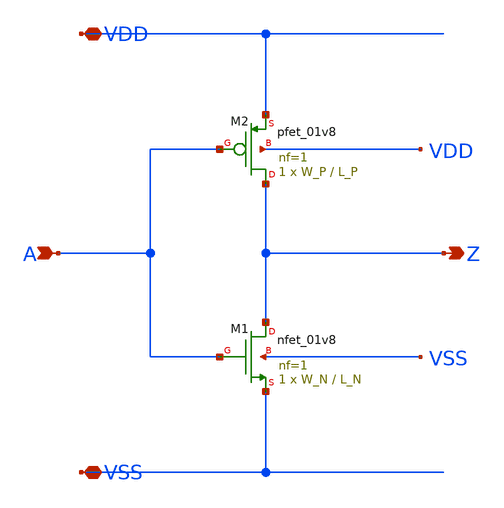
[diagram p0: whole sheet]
** sch_path: pipeline/analog/inv/inv.sch
**.subckt inv A Z VDD VSS
*.ipin A
*.opin Z
*.iopin VDD
*.iopin VSS
XM1 Z A VSS VSS sky130_fd_pr__nfet_01v8 L=L_N W=W_N nf=1 ad='int((nf+1)/2) * W/nf * 0.29' as='int((nf+2)/2) * W/nf * 0.29'
+ pd='2*int((nf+1)/2) * (W/nf + 0.29)' ps='2*int((nf+2)/2) * (W/nf + 0.29)' nrd='0.29 / W' nrs='0.29 / W'
+ sa=0 sb=0 sd=0 mult=1 m=1
XM2 Z A VDD VDD sky130_fd_pr__pfet_01v8 L=L_P W=W_P nf=1 ad='int((nf+1)/2) * W/nf * 0.29' as='int((nf+2)/2) * W/nf * 0.29'
+ pd='2*int((nf+1)/2) * (W/nf + 0.29)' ps='2*int((nf+2)/2) * (W/nf + 0.29)' nrd='0.29 / W' nrs='0.29 / W'
+ sa=0 sb=0 sd=0 mult=1 m=1
**.ends
.end
